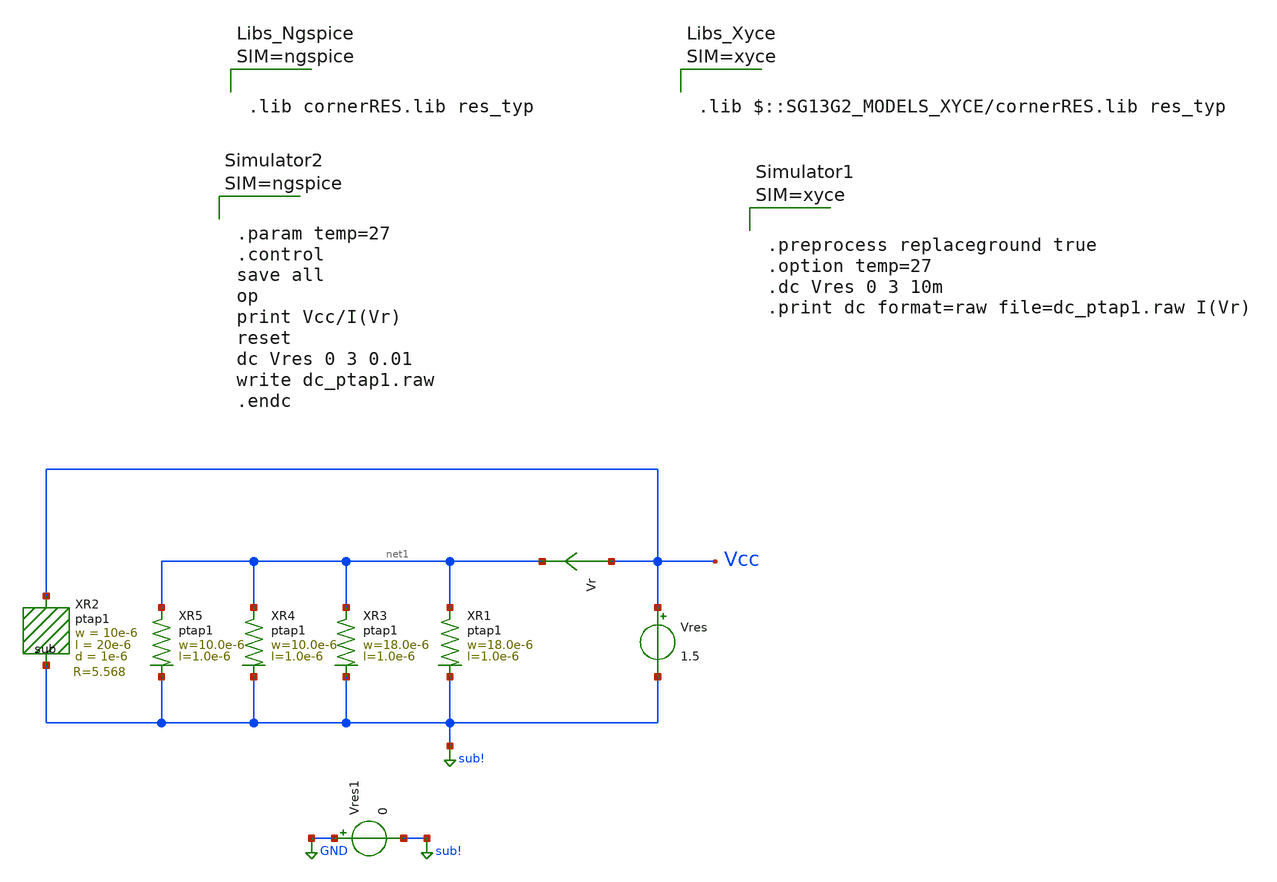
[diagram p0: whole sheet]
** sch_path: ihp-sg13g2/libs.tech/xschem/sg13g2_tests_xyce/dc_ptap1.sch
* Copyright 2023 IHP PDK Authors
**.subckt dc_ptap1
Vres Vcc sub! 1.5
Vr Vcc net1 0
.save i(vr)
XR2 Vcc sub! ptap1 R=5.568 w=10e-6 l=20e-6 d=1e-6
XR3 sub! net1 ptap1 R=17.5 w=18.0e-6 l=1.0e-6
XR5 sub! net1 ptap1 R=30.62 w=10.0e-6 l=1.0e-6
XR4 sub! net1 ptap1 R=30.62 w=10.0e-6 l=1.0e-6
XR1 sub! net1 ptap1 R=17.5 w=18.0e-6 l=1.0e-6
Vres1 GND sub! 0
**** begin user architecture code









.lib cornerRES.lib res_typ






.param temp=27
.control
save all
op
print Vcc/I(Vr)
reset
dc Vres 0 3 0.01
write dc_ptap1.raw
.endc



**** end user architecture code
**.ends
.GLOBAL GND
.GLOBAL sub!
.end
